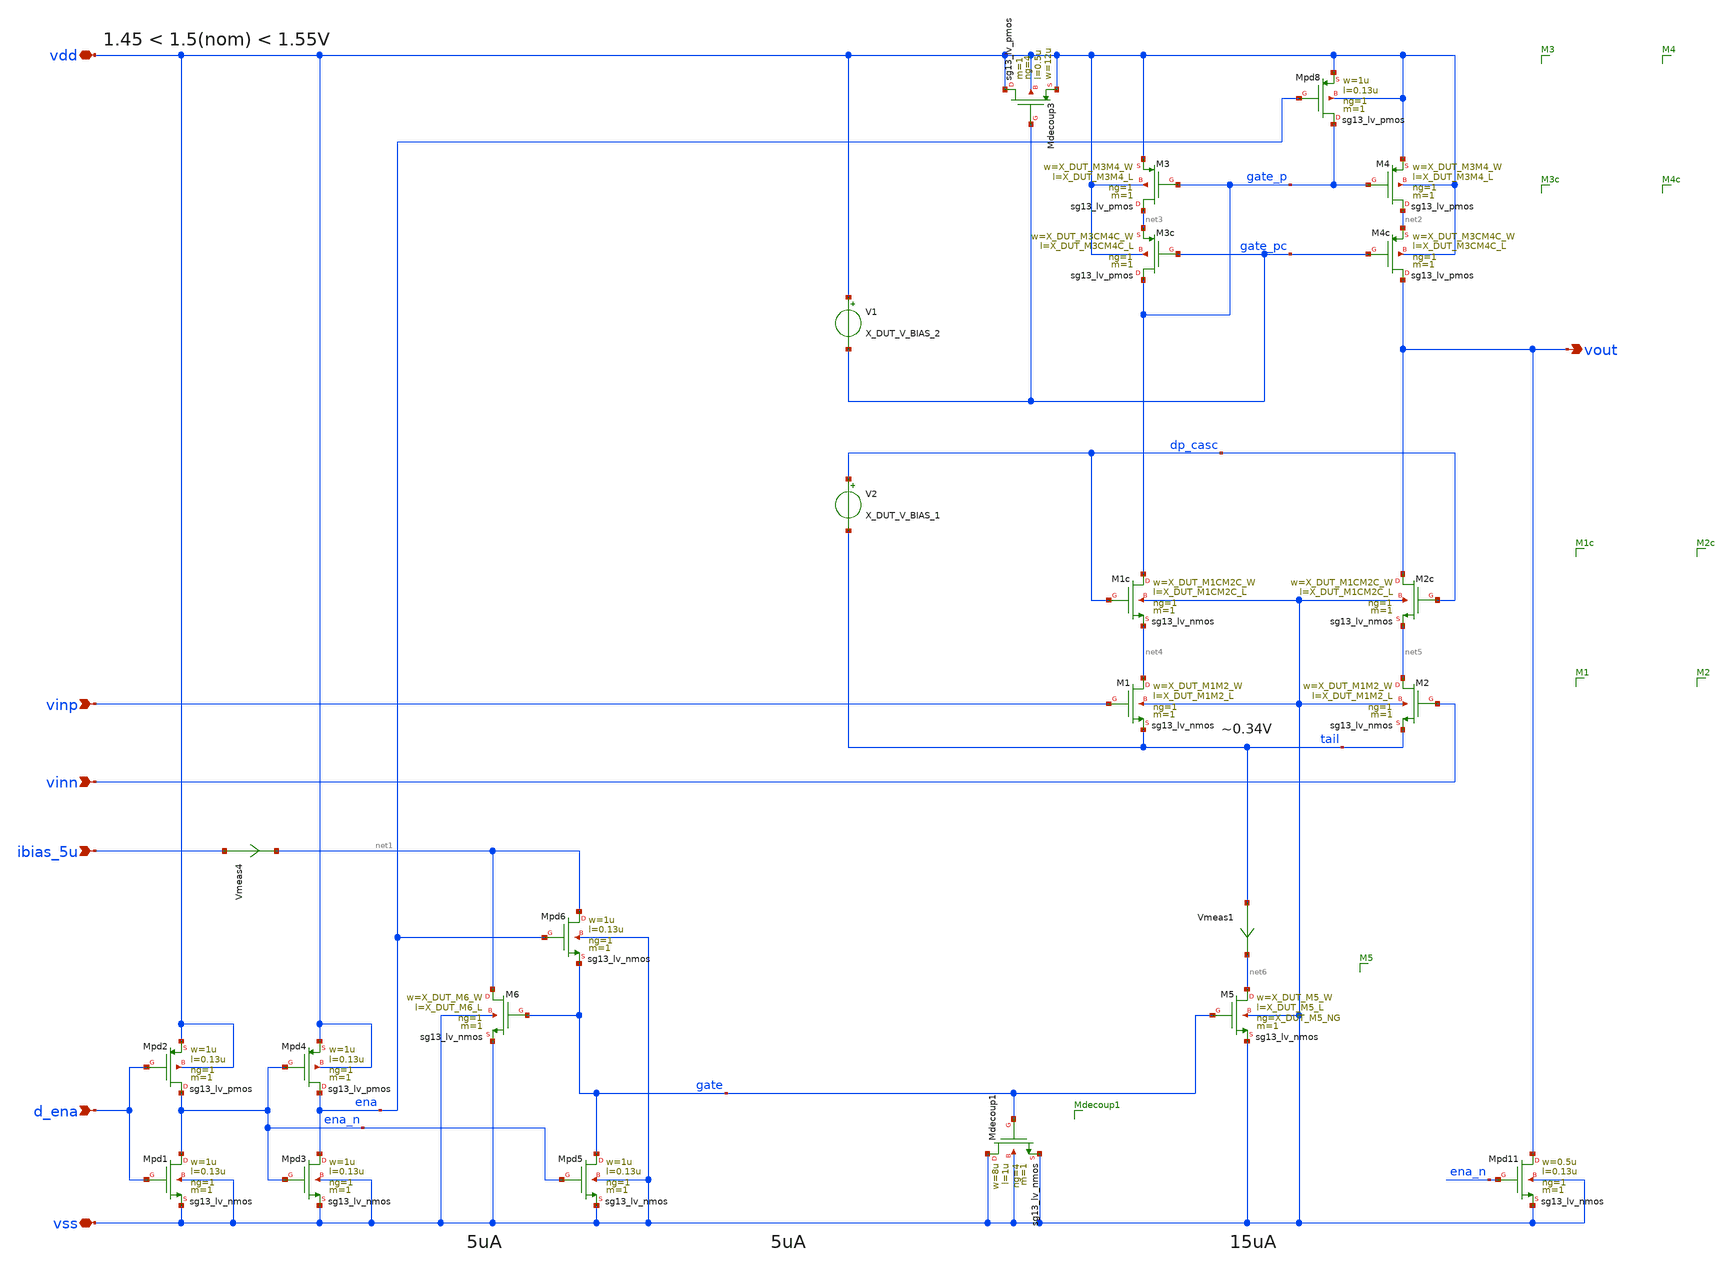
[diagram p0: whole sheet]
** sch_path: analog-db/circuits/amp_018_telescopic_cascode/pdk/ihp-sg13g2/schematic/ota-improved.sch
* (c) 2024-2025 Harald Pretl, Apache-2.0 license
**.subckt ota-improved ibias_5u vdd vss vinp vinn vout d_ena
*.ipin ibias_5u
*.iopin vdd
*.iopin vss
*.ipin vinp
*.ipin vinn
*.opin vout
*.ipin d_ena
XM5 net6 gate vss vss sg13_lv_nmos w=X_DUT_M5_W l=X_DUT_M5_L ng=X_DUT_M5_NG m=1 mm_ok=1
XM4 net2 gate_p vdd vdd sg13_lv_pmos w=X_DUT_M3M4_W l=X_DUT_M3M4_L ng=1 m=1 mm_ok=1
XM1 net4 vinp tail vss sg13_lv_nmos w=X_DUT_M1M2_W l=X_DUT_M1M2_L ng=1 m=1 mm_ok=1
XM2 net5 vinn tail vss sg13_lv_nmos w=X_DUT_M1M2_W l=X_DUT_M1M2_L ng=1 m=1 mm_ok=1
XM3 net3 gate_p vdd vdd sg13_lv_pmos w=X_DUT_M3M4_W l=X_DUT_M3M4_L ng=1 m=1 mm_ok=1
XM6 net1 gate vss vss sg13_lv_nmos w=X_DUT_M6_W l=X_DUT_M6_L ng=1 m=1 mm_ok=1
XMpd5 gate ena_n vss vss sg13_lv_nmos w=1u l=0.13u ng=1 m=1 mm_ok=1
XMpd3 ena ena_n vss vss sg13_lv_nmos w=1u l=0.13u ng=1 m=1 mm_ok=1
XMpd4 ena ena_n vdd vdd sg13_lv_pmos w=1u l=0.13u ng=1 m=1 mm_ok=1
XMpd6 net1 ena gate vss sg13_lv_nmos w=1u l=0.13u ng=1 m=1 mm_ok=1
XM2c vout dp_casc net5 vss sg13_lv_nmos w=X_DUT_M1CM2C_W l=X_DUT_M1CM2C_L ng=1 m=1 mm_ok=1
XM1c gate_p dp_casc net4 vss sg13_lv_nmos w=X_DUT_M1CM2C_W l=X_DUT_M1CM2C_L ng=1 m=1 mm_ok=1
XM4c vout gate_pc net2 vdd sg13_lv_pmos w=X_DUT_M3CM4C_W l=X_DUT_M3CM4C_L ng=1 m=1 mm_ok=1
XM3c gate_p gate_pc net3 vdd sg13_lv_pmos w=X_DUT_M3CM4C_W l=X_DUT_M3CM4C_L ng=1 m=1 mm_ok=1
XMpd8 gate_p ena vdd vdd sg13_lv_pmos w=1u l=0.13u ng=1 m=1 mm_ok=1
Vmeas1 tail net6 0
XMpd1 ena_n d_ena vss vss sg13_lv_nmos w=1u l=0.13u ng=1 m=1 mm_ok=1
XMpd2 ena_n d_ena vdd vdd sg13_lv_pmos w=1u l=0.13u ng=1 m=1 mm_ok=1
Vmeas4 ibias_5u net1 0
XMpd11 vout ena_n vss vss sg13_lv_nmos w=0.5u l=0.13u ng=1 m=1 mm_ok=1
XMdecoup1 vss gate vss vss sg13_lv_nmos w=8u l=1u ng=4 m=1 mm_ok=1
XMdecoup3 vdd gate_pc vdd vdd sg13_lv_pmos w=12u l=0.5u ng=4 m=1 mm_ok=1
V1 vdd gate_pc X_DUT_V_BIAS_2
V2 dp_casc tail X_DUT_V_BIAS_1
**.ends
.end
